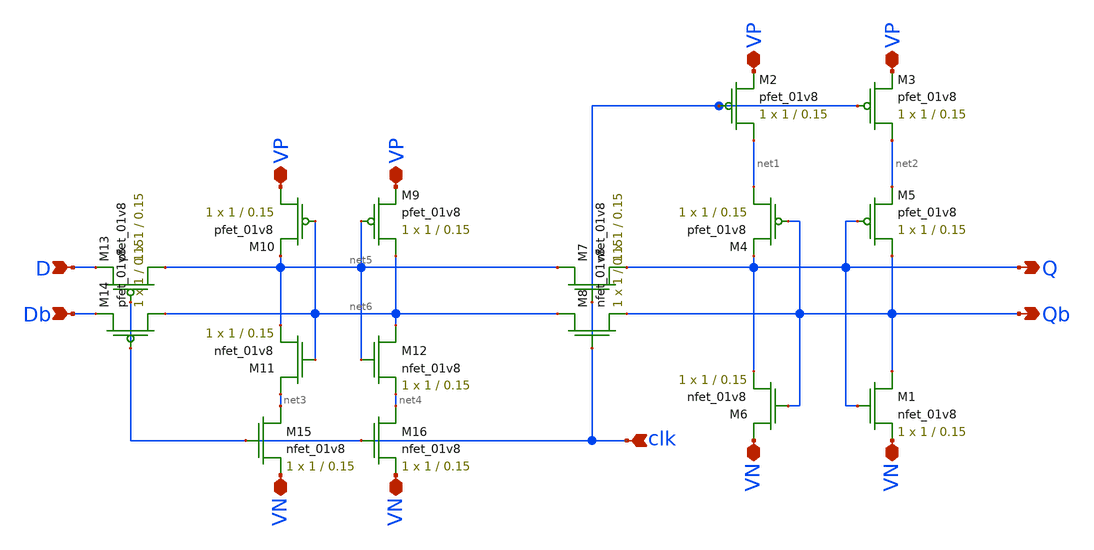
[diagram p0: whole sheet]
** sch_path: Miniproject2/dflipflop.sch
**.subckt dflipflop VP clk D Db Q Qb VP VN VN VN VN VP VP
*.iopin VP
*.ipin clk
*.ipin D
*.ipin Db
*.opin Q
*.opin Qb
*.iopin VP
*.iopin VN
*.iopin VN
*.iopin VN
*.iopin VN
*.iopin VP
*.iopin VP
XM1 Qb Q VN GND sky130_fd_pr__nfet_01v8 L=0.15 W=1 nf=1 ad='int((nf+1)/2) * W/nf * 0.29' as='int((nf+2)/2) * W/nf * 0.29'
+ pd='2*int((nf+1)/2) * (W/nf + 0.29)' ps='2*int((nf+2)/2) * (W/nf + 0.29)' nrd='0.29 / W' nrs='0.29 / W'
+ sa=0 sb=0 sd=0 mult=1 m=1
XM2 net1 clk VP VDD sky130_fd_pr__pfet_01v8 L=0.15 W=1 nf=1 ad='int((nf+1)/2) * W/nf * 0.29' as='int((nf+2)/2) * W/nf * 0.29'
+ pd='2*int((nf+1)/2) * (W/nf + 0.29)' ps='2*int((nf+2)/2) * (W/nf + 0.29)' nrd='0.29 / W' nrs='0.29 / W'
+ sa=0 sb=0 sd=0 mult=1 m=1
XM3 net2 clk VP VDD sky130_fd_pr__pfet_01v8 L=0.15 W=1 nf=1 ad='int((nf+1)/2) * W/nf * 0.29' as='int((nf+2)/2) * W/nf * 0.29'
+ pd='2*int((nf+1)/2) * (W/nf + 0.29)' ps='2*int((nf+2)/2) * (W/nf + 0.29)' nrd='0.29 / W' nrs='0.29 / W'
+ sa=0 sb=0 sd=0 mult=1 m=1
XM4 net1 Qb Q VDD sky130_fd_pr__pfet_01v8 L=0.15 W=1 nf=1 ad='int((nf+1)/2) * W/nf * 0.29' as='int((nf+2)/2) * W/nf * 0.29'
+ pd='2*int((nf+1)/2) * (W/nf + 0.29)' ps='2*int((nf+2)/2) * (W/nf + 0.29)' nrd='0.29 / W' nrs='0.29 / W'
+ sa=0 sb=0 sd=0 mult=1 m=1
XM5 Qb Q net2 VDD sky130_fd_pr__pfet_01v8 L=0.15 W=1 nf=1 ad='int((nf+1)/2) * W/nf * 0.29' as='int((nf+2)/2) * W/nf * 0.29'
+ pd='2*int((nf+1)/2) * (W/nf + 0.29)' ps='2*int((nf+2)/2) * (W/nf + 0.29)' nrd='0.29 / W' nrs='0.29 / W'
+ sa=0 sb=0 sd=0 mult=1 m=1
XM6 VN Qb Q GND sky130_fd_pr__nfet_01v8 L=0.15 W=1 nf=1 ad='int((nf+1)/2) * W/nf * 0.29' as='int((nf+2)/2) * W/nf * 0.29'
+ pd='2*int((nf+1)/2) * (W/nf + 0.29)' ps='2*int((nf+2)/2) * (W/nf + 0.29)' nrd='0.29 / W' nrs='0.29 / W'
+ sa=0 sb=0 sd=0 mult=1 m=1
XM7 net5 clk Q GND sky130_fd_pr__nfet_01v8 L=0.15 W=1 nf=1 ad='int((nf+1)/2) * W/nf * 0.29' as='int((nf+2)/2) * W/nf * 0.29'
+ pd='2*int((nf+1)/2) * (W/nf + 0.29)' ps='2*int((nf+2)/2) * (W/nf + 0.29)' nrd='0.29 / W' nrs='0.29 / W'
+ sa=0 sb=0 sd=0 mult=1 m=1
XM8 net6 clk Qb GND sky130_fd_pr__nfet_01v8 L=0.15 W=1 nf=1 ad='int((nf+1)/2) * W/nf * 0.29' as='int((nf+2)/2) * W/nf * 0.29'
+ pd='2*int((nf+1)/2) * (W/nf + 0.29)' ps='2*int((nf+2)/2) * (W/nf + 0.29)' nrd='0.29 / W' nrs='0.29 / W'
+ sa=0 sb=0 sd=0 mult=1 m=1
XM9 net6 net5 VP VDD sky130_fd_pr__pfet_01v8 L=0.15 W=1 nf=1 ad='int((nf+1)/2) * W/nf * 0.29' as='int((nf+2)/2) * W/nf * 0.29'
+ pd='2*int((nf+1)/2) * (W/nf + 0.29)' ps='2*int((nf+2)/2) * (W/nf + 0.29)' nrd='0.29 / W' nrs='0.29 / W'
+ sa=0 sb=0 sd=0 mult=1 m=1
XM10 VP net6 net5 VDD sky130_fd_pr__pfet_01v8 L=0.15 W=1 nf=1 ad='int((nf+1)/2) * W/nf * 0.29' as='int((nf+2)/2) * W/nf * 0.29'
+ pd='2*int((nf+1)/2) * (W/nf + 0.29)' ps='2*int((nf+2)/2) * (W/nf + 0.29)' nrd='0.29 / W' nrs='0.29 / W'
+ sa=0 sb=0 sd=0 mult=1 m=1
XM11 net3 net6 net5 GND sky130_fd_pr__nfet_01v8 L=0.15 W=1 nf=1 ad='int((nf+1)/2) * W/nf * 0.29' as='int((nf+2)/2) * W/nf * 0.29'
+ pd='2*int((nf+1)/2) * (W/nf + 0.29)' ps='2*int((nf+2)/2) * (W/nf + 0.29)' nrd='0.29 / W' nrs='0.29 / W'
+ sa=0 sb=0 sd=0 mult=1 m=1
XM12 net6 net5 net4 GND sky130_fd_pr__nfet_01v8 L=0.15 W=1 nf=1 ad='int((nf+1)/2) * W/nf * 0.29' as='int((nf+2)/2) * W/nf * 0.29'
+ pd='2*int((nf+1)/2) * (W/nf + 0.29)' ps='2*int((nf+2)/2) * (W/nf + 0.29)' nrd='0.29 / W' nrs='0.29 / W'
+ sa=0 sb=0 sd=0 mult=1 m=1
XM13 net5 clk D VDD sky130_fd_pr__pfet_01v8 L=0.15 W=1 nf=1 ad='int((nf+1)/2) * W/nf * 0.29' as='int((nf+2)/2) * W/nf * 0.29'
+ pd='2*int((nf+1)/2) * (W/nf + 0.29)' ps='2*int((nf+2)/2) * (W/nf + 0.29)' nrd='0.29 / W' nrs='0.29 / W'
+ sa=0 sb=0 sd=0 mult=1 m=1
XM14 net6 clk Db VDD sky130_fd_pr__pfet_01v8 L=0.15 W=1 nf=1 ad='int((nf+1)/2) * W/nf * 0.29' as='int((nf+2)/2) * W/nf * 0.29'
+ pd='2*int((nf+1)/2) * (W/nf + 0.29)' ps='2*int((nf+2)/2) * (W/nf + 0.29)' nrd='0.29 / W' nrs='0.29 / W'
+ sa=0 sb=0 sd=0 mult=1 m=1
XM15 net3 clk VN GND sky130_fd_pr__nfet_01v8 L=0.15 W=1 nf=1 ad='int((nf+1)/2) * W/nf * 0.29' as='int((nf+2)/2) * W/nf * 0.29'
+ pd='2*int((nf+1)/2) * (W/nf + 0.29)' ps='2*int((nf+2)/2) * (W/nf + 0.29)' nrd='0.29 / W' nrs='0.29 / W'
+ sa=0 sb=0 sd=0 mult=1 m=1
XM16 net4 clk VN GND sky130_fd_pr__nfet_01v8 L=0.15 W=1 nf=1 ad='int((nf+1)/2) * W/nf * 0.29' as='int((nf+2)/2) * W/nf * 0.29'
+ pd='2*int((nf+1)/2) * (W/nf + 0.29)' ps='2*int((nf+2)/2) * (W/nf + 0.29)' nrd='0.29 / W' nrs='0.29 / W'
+ sa=0 sb=0 sd=0 mult=1 m=1
**.ends
.end
